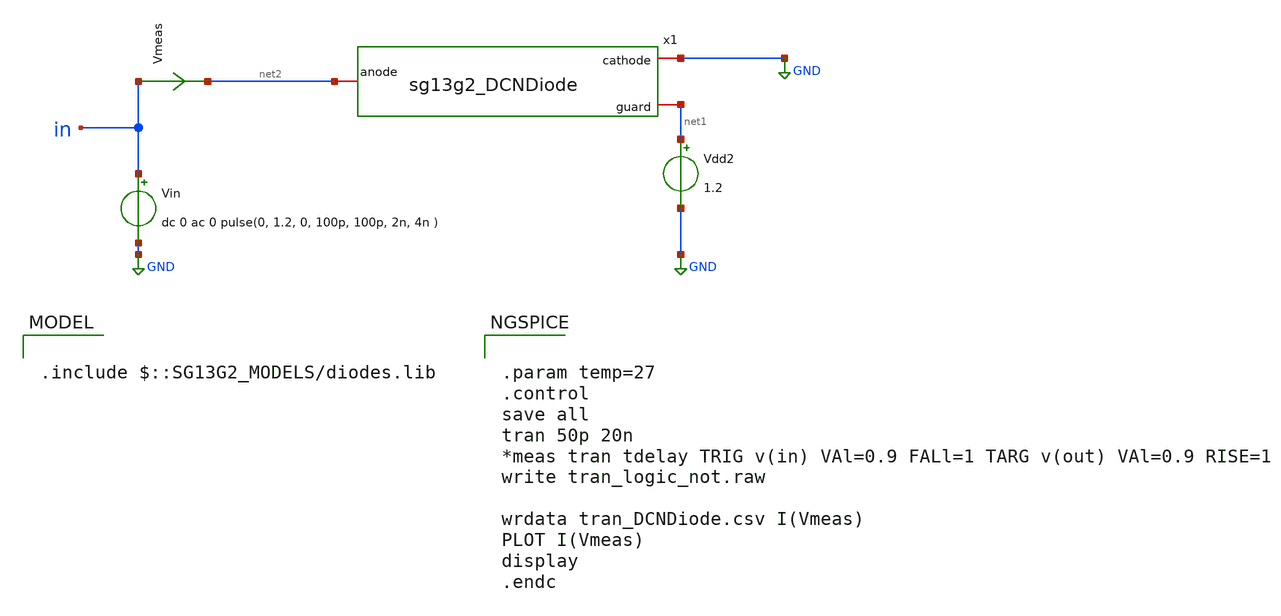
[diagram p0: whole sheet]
** sch_path: ihp-sg13g2/libs.ref/sg13g2_io/xschem/io_testbench/sg13g2_io_DCNDiode_tb.sch
* Copyright 2023 IHP PDK Authors
**.subckt sg13g2_io_DCNDiode_tb
x1 GND net2 net1 sg13g2_DCNDiode
Vdd2 net1 GND 1.2
Vin in GND dc 0 ac 0 pulse(0, 1.2, 0, 100p, 100p, 2n, 4n )
Vmeas in net2 0
.save i(vmeas)
**** begin user architecture code


.param temp=27
.control
save all
tran 50p 20n
*meas tran tdelay TRIG v(in) VAl=0.9 FALl=1 TARG v(out) VAl=0.9 RISE=1
write tran_logic_not.raw

wrdata tran_DCNDiode.csv I(Vmeas)
PLOT I(Vmeas)
display
.endc



.include $::SG13G2_MODELS/diodes.lib

**** end user architecture code
**.ends

* expanding   symbol:  sg13g2_DCNDiode.sym # of pins=3
** sym_path: ihp-sg13g2/libs.ref/sg13g2_io/xschem/sg13g2_DCNDiode.sym
** sch_path: ihp-sg13g2/libs.ref/sg13g2_io/xschem/sg13g2_DCNDiode.sch
.subckt sg13g2_DCNDiode cathode anode guard
*.iopin cathode
*.iopin anode
*.iopin guard
XD1 anode cathode dantenna l=1.26u w=27.78u
XD2 anode cathode dantenna l=27.78u w=1.26u
.ends

.GLOBAL GND
.end
